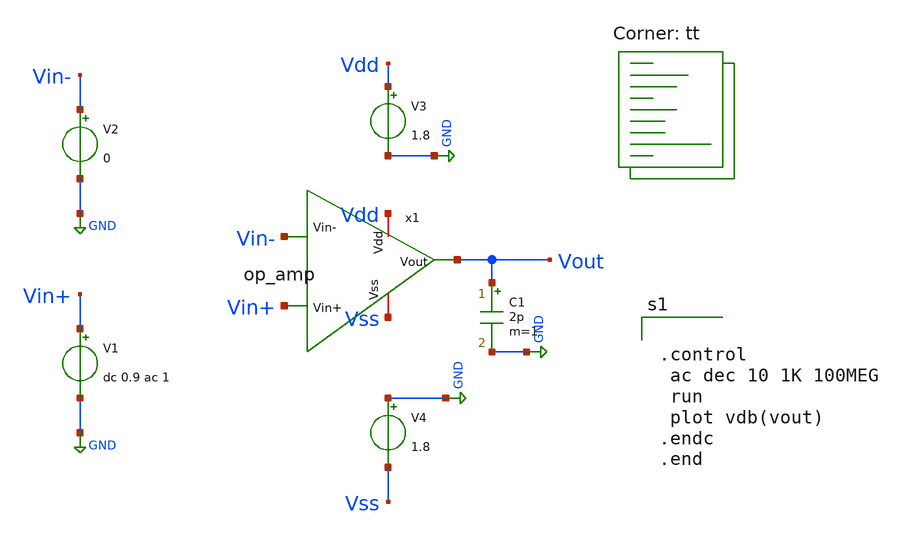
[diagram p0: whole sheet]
** sch_path: xschem/tb_opamp.sch
**.subckt tb_opamp
x1 Vdd Vin- Vout Vin+ Vss op_amp
V1 Vin+ GND dc 0.9 ac 1
V2 Vin- GND 0
V3 Vdd GND 1.8
V4 GND Vss 1.8
C1 Vout GND 2p m=1
**** begin user architecture code
.lib $::SKYWATER_MODELS/sky130.lib.spice tt


.control
 ac dec 10 1K 100MEG
 run
 plot vdb(vout)
.endc
.end

**** end user architecture code
**.ends

* expanding   symbol:  op_amp.sym # of pins=5
** sym_path: xschem/op_amp.sym
** sch_path: xschem/op_amp.sch
.subckt op_amp Vdd Vin- Vout Vin+ Vss
*.ipin Vin-
*.ipin Vin+
*.iopin Vss
*.opin Vout
*.iopin Vdd
XM1 net1 net1 Vss Vss sky130_fd_pr__nfet_01v8 L=0.18 W=1.59 nf=1 ad='int((1 + 1)/2) * 1.59 / 1 * 0.29'
+ as='int((1 + 2)/2) * 1.59 / 1 * 0.29' pd='2*int((1 + 1)/2) * (1.59 / 1 + 0.29)' ps='2*int((1 + 2)/2) * (1.59 / 1 + 0.29)'
+ nrd='0.29 / 1.59 ' nrs='0.29 / 1.59 ' sa=0 sb=0 sd=0 mult=1 m=1
XM3 net2 net1 Vss Vss sky130_fd_pr__nfet_01v8 L=0.18 W=1.59 nf=1 ad='int((1 + 1)/2) * 1.59 / 1 * 0.29'
+ as='int((1 + 2)/2) * 1.59 / 1 * 0.29' pd='2*int((1 + 1)/2) * (1.59 / 1 + 0.29)' ps='2*int((1 + 2)/2) * (1.59 / 1 + 0.29)'
+ nrd='0.29 / 1.59 ' nrs='0.29 / 1.59 ' sa=0 sb=0 sd=0 mult=1 m=1
XM9 Vout net1 Vss Vss sky130_fd_pr__nfet_01v8 L=0.18 W=10.6 nf=1 ad='int((1 + 1)/2) * 10.6 / 1 * 0.29'
+ as='int((1 + 2)/2) * 10.6 / 1 * 0.29' pd='2*int((1 + 1)/2) * (10.6 / 1 + 0.29)' ps='2*int((1 + 2)/2) * (10.6 / 1 + 0.29)'
+ nrd='0.29 / 10.6 ' nrs='0.29 / 10.6 ' sa=0 sb=0 sd=0 mult=1 m=1
XM10 net5 Vin- net2 Vss sky130_fd_pr__nfet_01v8 L=0.18 W=0.6 nf=1 ad='int((1 + 1)/2) * 0.6 / 1 * 0.29'
+ as='int((1 + 2)/2) * 0.6 / 1 * 0.29' pd='2*int((1 + 1)/2) * (0.6 / 1 + 0.29)' ps='2*int((1 + 2)/2) * (0.6 / 1 + 0.29)'
+ nrd='0.29 / 0.6 ' nrs='0.29 / 0.6 ' sa=0 sb=0 sd=0 mult=1 m=1
XM11 net6 Vin+ net2 Vss sky130_fd_pr__nfet_01v8 L=0.18 W=0.6 nf=1 ad='int((1 + 1)/2) * 0.6 / 1 * 0.29'
+ as='int((1 + 2)/2) * 0.6 / 1 * 0.29' pd='2*int((1 + 1)/2) * (0.6 / 1 + 0.29)' ps='2*int((1 + 2)/2) * (0.6 / 1 + 0.29)'
+ nrd='0.29 / 0.6 ' nrs='0.29 / 0.6 ' sa=0 sb=0 sd=0 mult=1 m=1
XM12 net3 net3 Vdd Vdd sky130_fd_pr__pfet_01v8 L=0.18 W=0.6 nf=1 ad='int((1 + 1)/2) * 0.6 / 1 * 0.29'
+ as='int((1 + 2)/2) * 0.6 / 1 * 0.29' pd='2*int((1 + 1)/2) * (0.6 / 1 + 0.29)' ps='2*int((1 + 2)/2) * (0.6 / 1 + 0.29)'
+ nrd='0.29 / 0.6 ' nrs='0.29 / 0.6 ' sa=0 sb=0 sd=0 mult=1 m=1
XM2 net4 net4 net3 Vdd sky130_fd_pr__pfet_01v8 L=0.18 W=0.6 nf=1 ad='int((1 + 1)/2) * 0.6 / 1 * 0.29'
+ as='int((1 + 2)/2) * 0.6 / 1 * 0.29' pd='2*int((1 + 1)/2) * (0.6 / 1 + 0.29)' ps='2*int((1 + 2)/2) * (0.6 / 1 + 0.29)'
+ nrd='0.29 / 0.6 ' nrs='0.29 / 0.6 ' sa=0 sb=0 sd=0 mult=1 m=1
XM4 net1 net1 net4 Vdd sky130_fd_pr__pfet_01v8 L=0.18 W=0.6 nf=1 ad='int((1 + 1)/2) * 0.6 / 1 * 0.29'
+ as='int((1 + 2)/2) * 0.6 / 1 * 0.29' pd='2*int((1 + 1)/2) * (0.6 / 1 + 0.29)' ps='2*int((1 + 2)/2) * (0.6 / 1 + 0.29)'
+ nrd='0.29 / 0.6 ' nrs='0.29 / 0.6 ' sa=0 sb=0 sd=0 mult=1 m=1
XM5 net6 net5 Vdd Vdd sky130_fd_pr__pfet_01v8 L=0.18 W=3 nf=1 ad='int((1 + 1)/2) * 3 / 1 * 0.29' as='int((1 + 2)/2) * 3 / 1 * 0.29'
+ pd='2*int((1 + 1)/2) * (3 / 1 + 0.29)' ps='2*int((1 + 2)/2) * (3 / 1 + 0.29)' nrd='0.29 / 3 ' nrs='0.29 / 3 '
+ sa=0 sb=0 sd=0 mult=1 m=1
XM6 net5 net5 Vdd Vdd sky130_fd_pr__pfet_01v8 L=0.18 W=3 nf=1 ad='int((1 + 1)/2) * 3 / 1 * 0.29' as='int((1 + 2)/2) * 3 / 1 * 0.29'
+ pd='2*int((1 + 1)/2) * (3 / 1 + 0.29)' ps='2*int((1 + 2)/2) * (3 / 1 + 0.29)' nrd='0.29 / 3 ' nrs='0.29 / 3 '
+ sa=0 sb=0 sd=0 mult=1 m=1
XM7 Vout net6 Vdd Vdd sky130_fd_pr__pfet_01v8 L=0.18 W=45 nf=1 ad='int((1 + 1)/2) * 45 / 1 * 0.29' as='int((1 + 2)/2) * 45 / 1 * 0.29'
+ pd='2*int((1 + 1)/2) * (45 / 1 + 0.29)' ps='2*int((1 + 2)/2) * (45 / 1 + 0.29)' nrd='0.29 / 45 ' nrs='0.29 / 45 '
+ sa=0 sb=0 sd=0 mult=1 m=1
C1 Vout net6 800f m=1
.ends

.GLOBAL GND
.end
